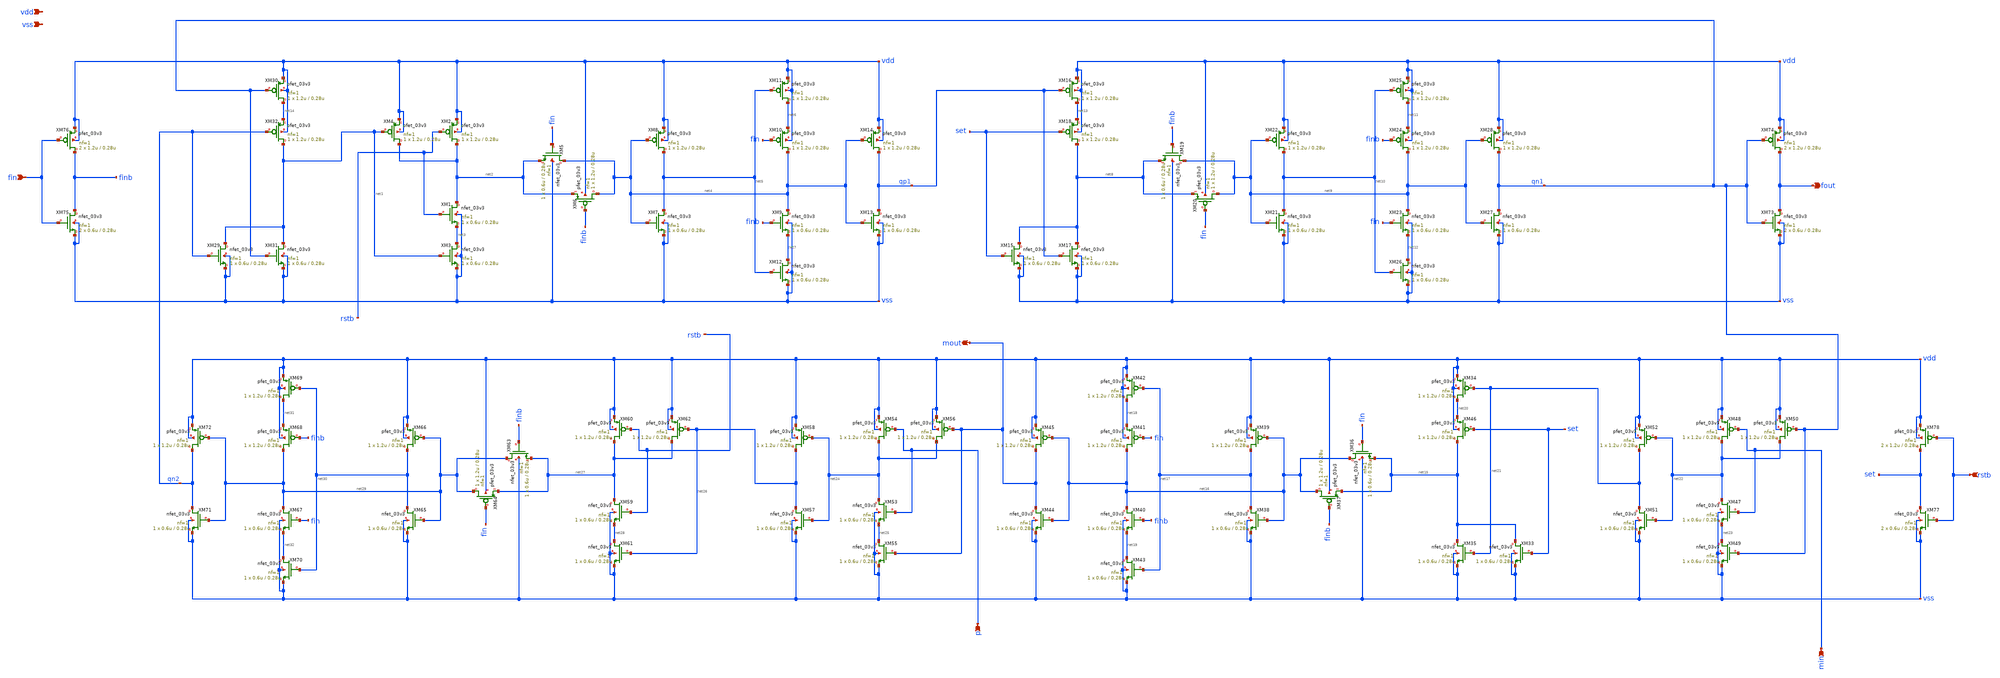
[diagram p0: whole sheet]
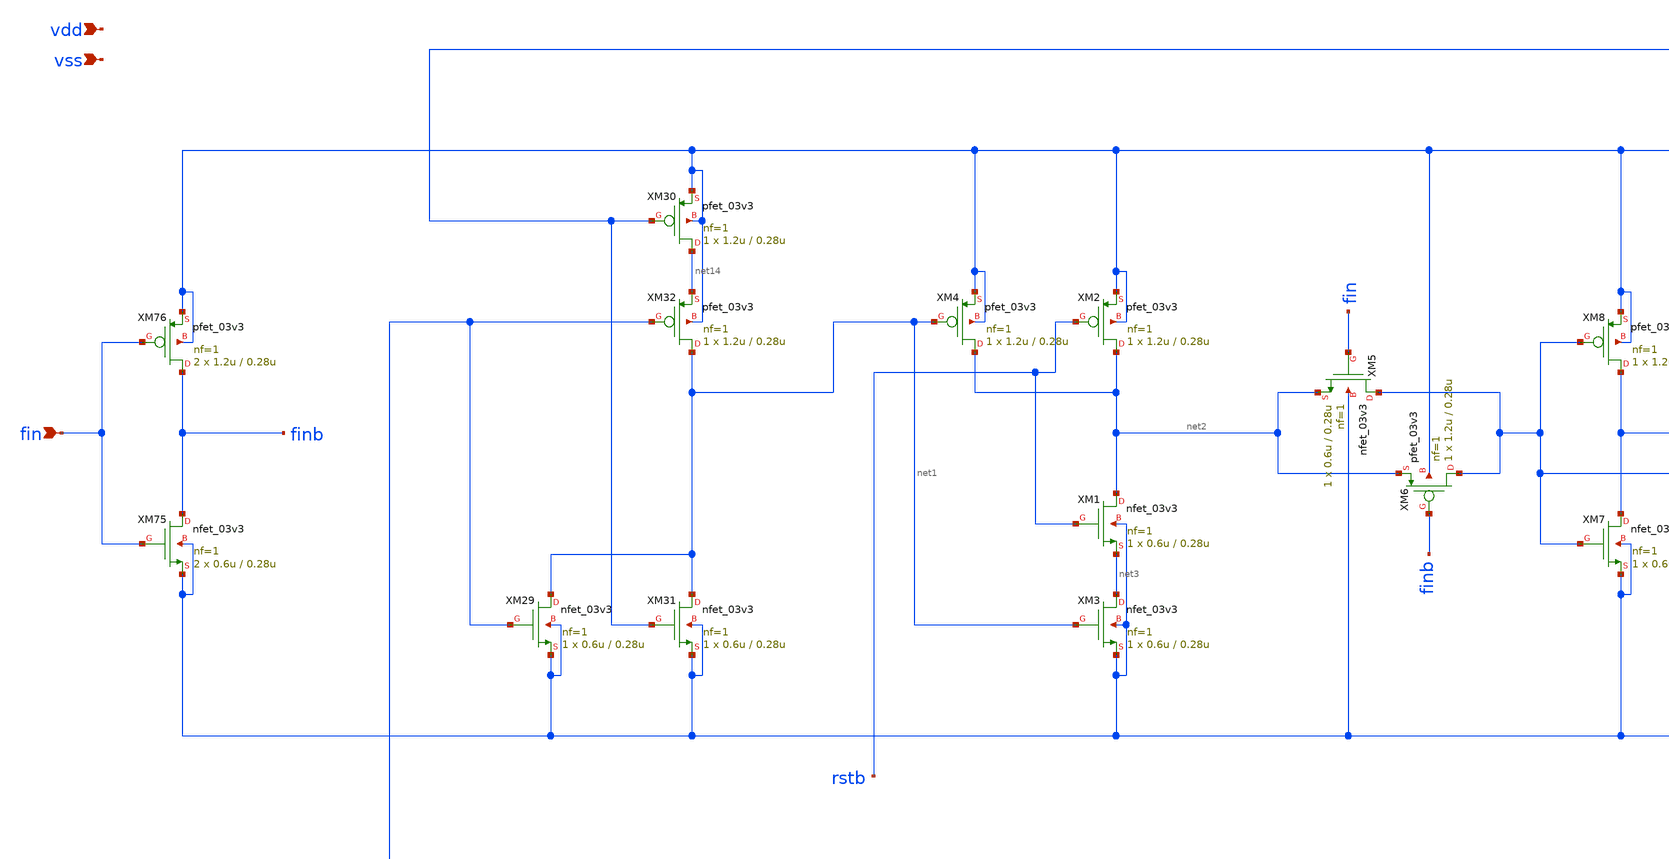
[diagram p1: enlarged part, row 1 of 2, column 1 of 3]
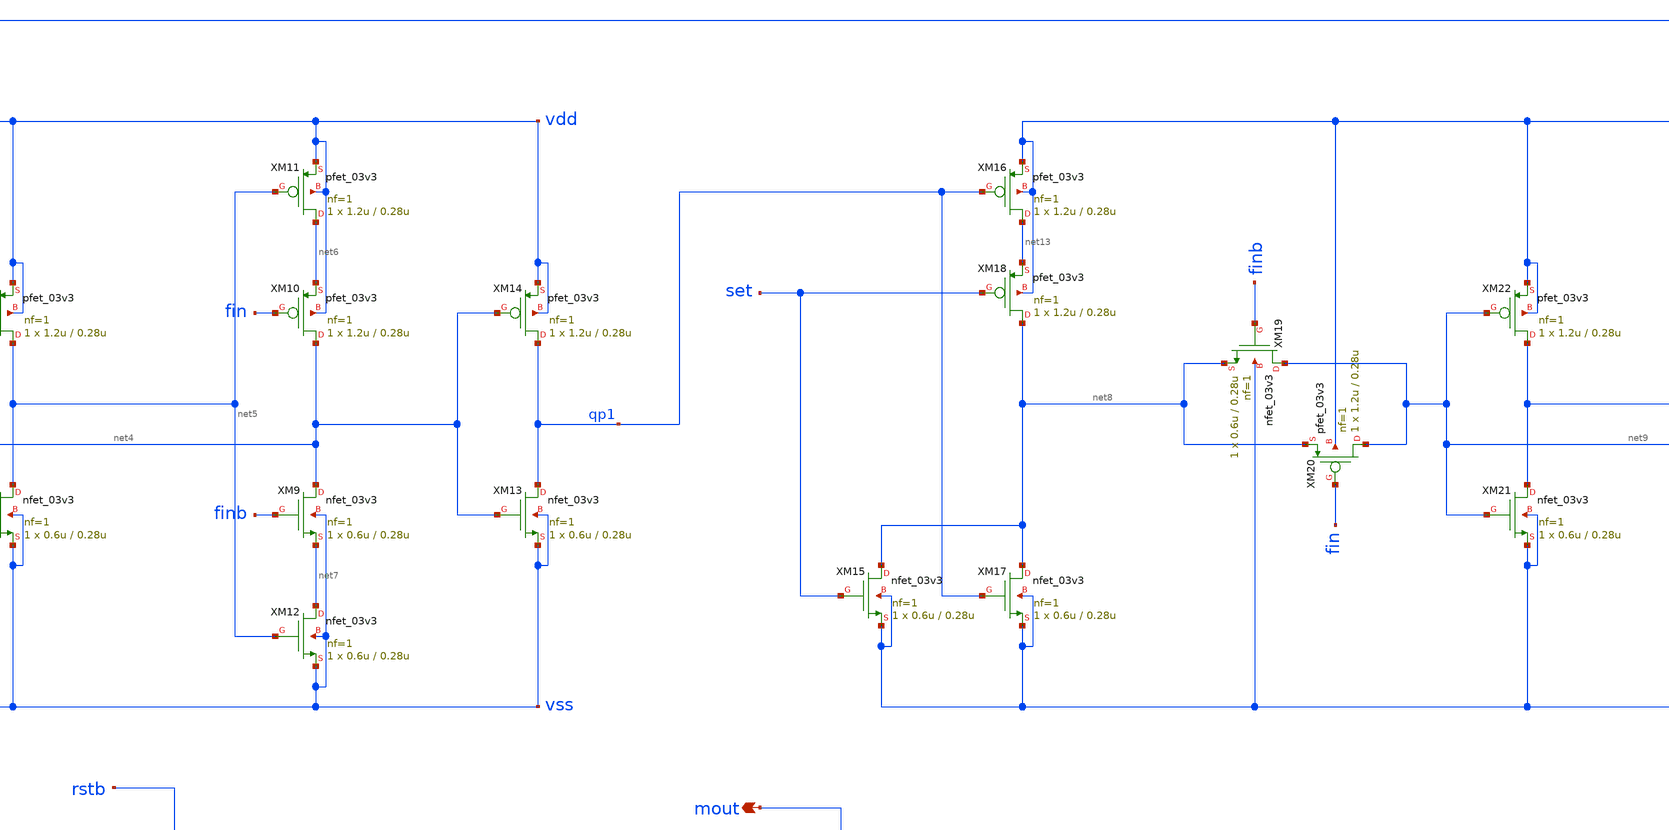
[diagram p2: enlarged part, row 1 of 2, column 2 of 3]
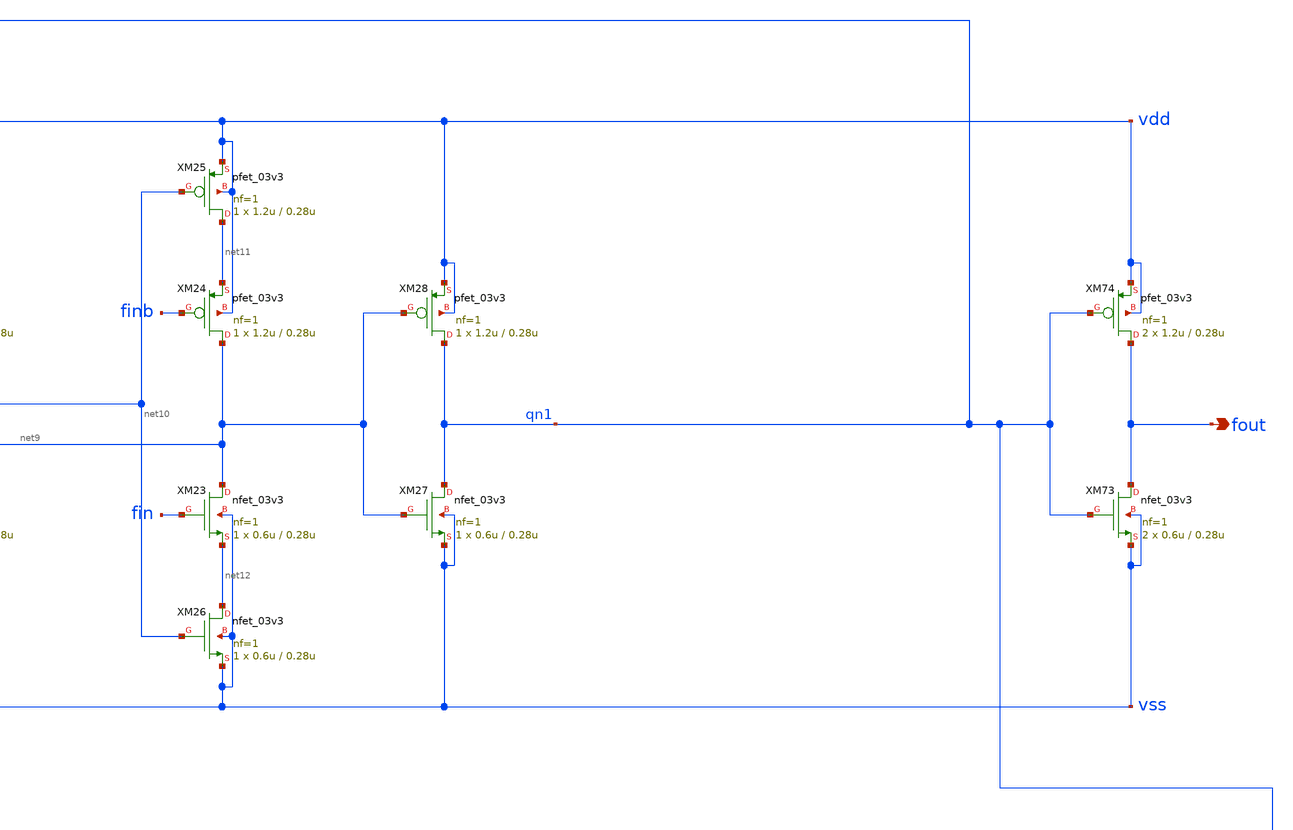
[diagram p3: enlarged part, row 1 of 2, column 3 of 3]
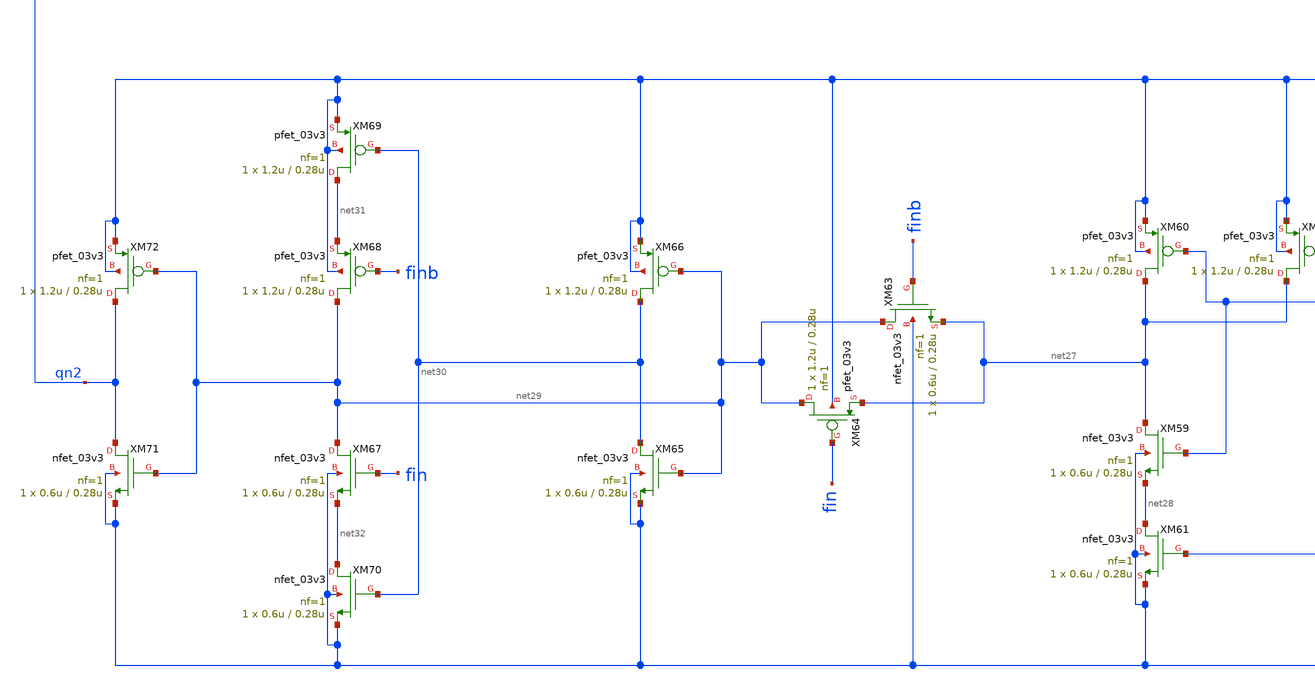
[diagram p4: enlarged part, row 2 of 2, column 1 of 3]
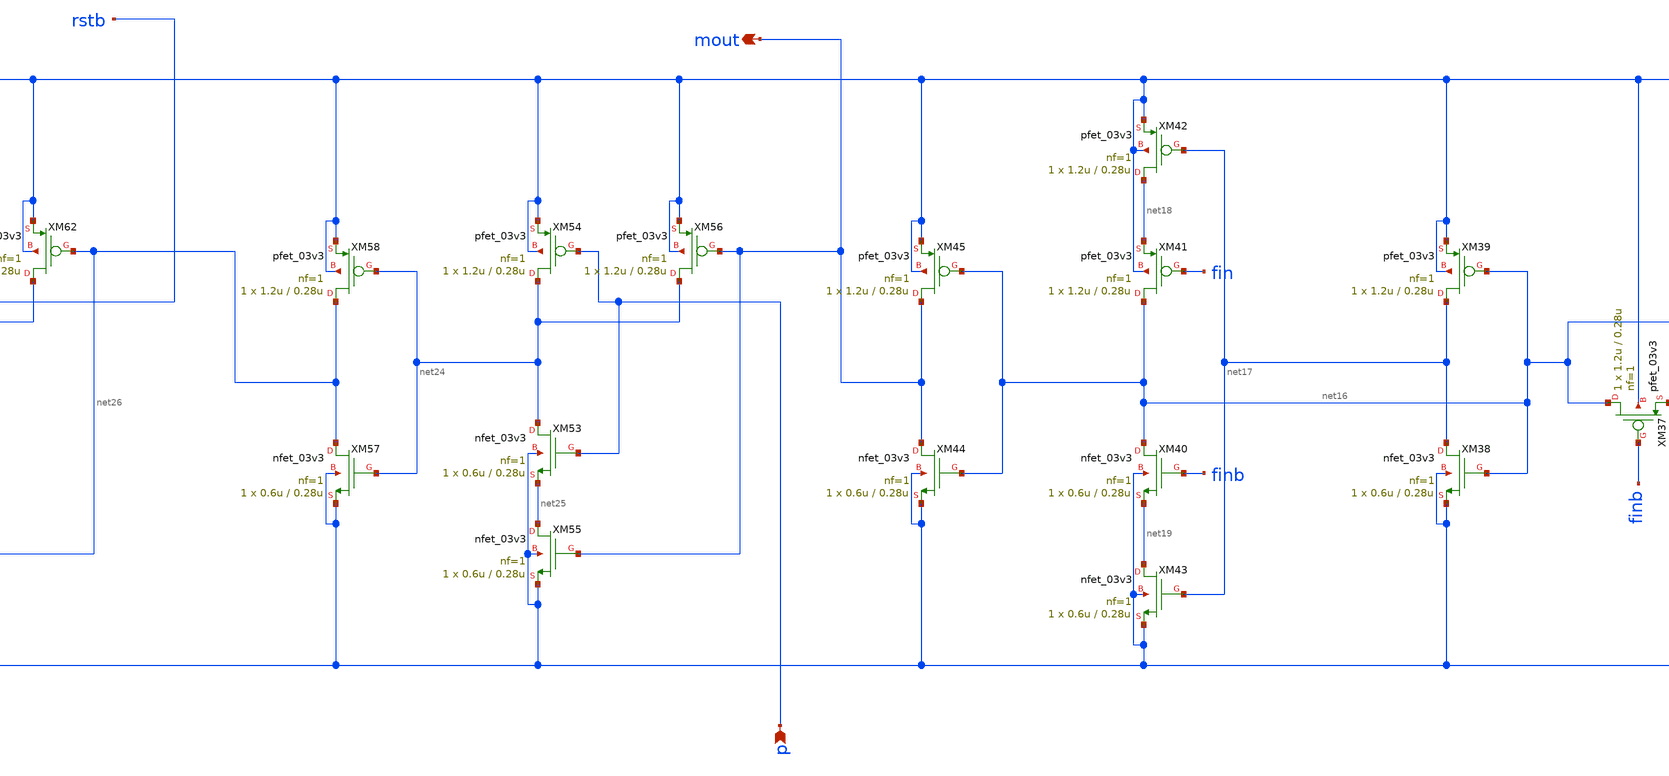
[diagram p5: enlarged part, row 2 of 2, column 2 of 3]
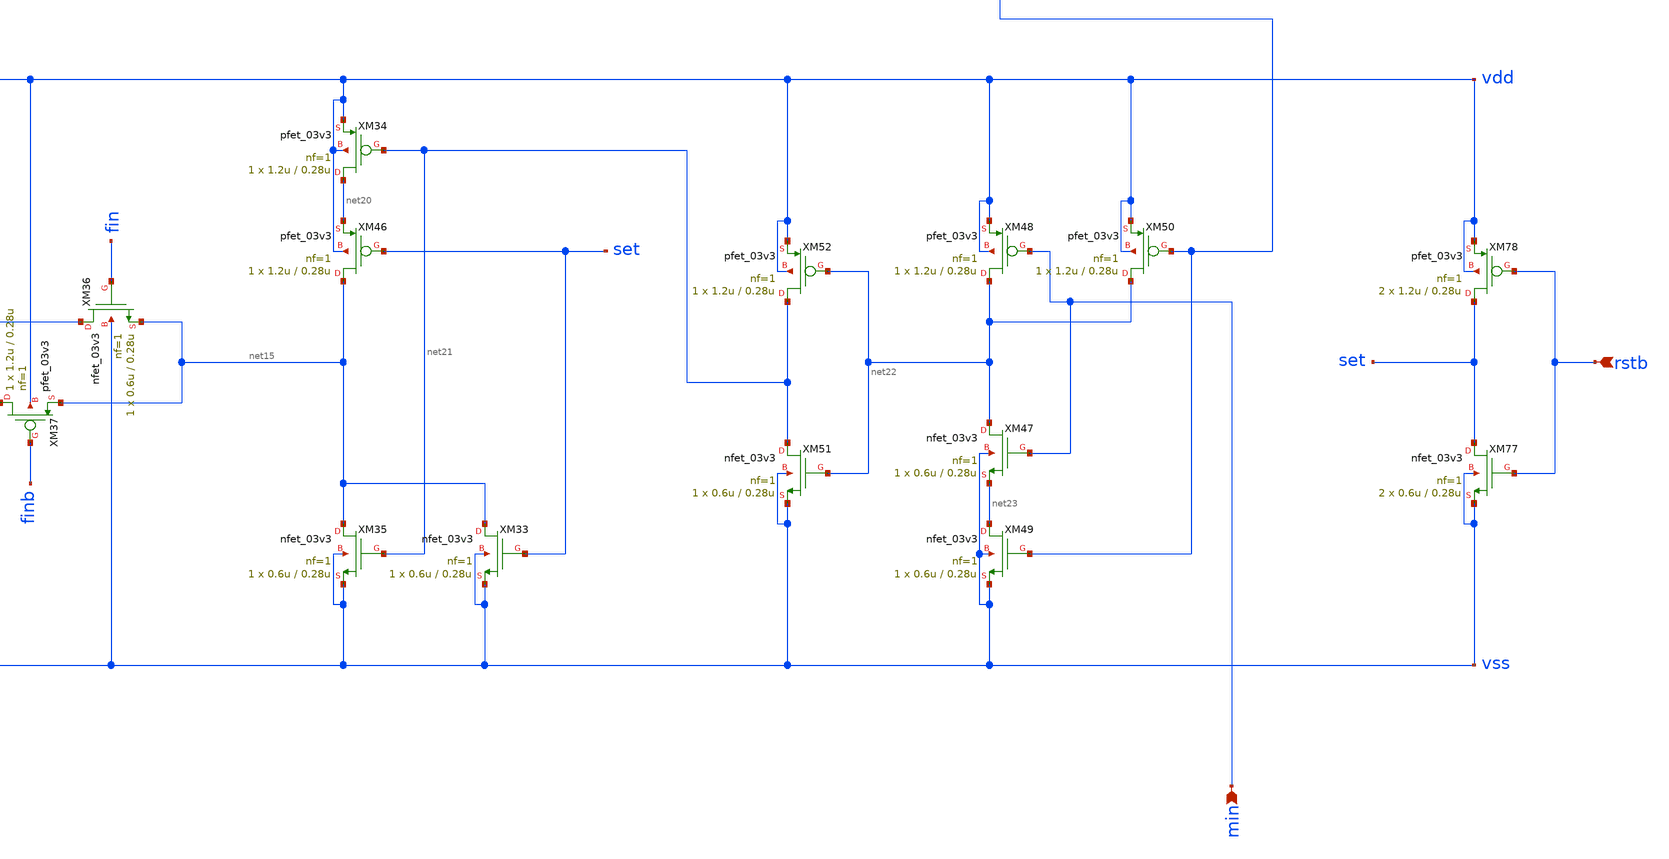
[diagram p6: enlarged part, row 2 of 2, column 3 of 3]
** sch_path: xschem/div23.sch
**.subckt div23 rstb fin p min fout mout vdd vss
*.ipin rstb
*.ipin fin
*.ipin p
*.ipin min
*.opin fout
*.opin mout
*.ipin vdd
*.ipin vss
XM1 net2 rstb net3 vss nfet_03v3 L=0.28u W=0.6u nf=1 ad='int((nf+1)/2) * W/nf * 0.18u' as='int((nf+2)/2) * W/nf * 0.18u'
+ pd='2*int((nf+1)/2) * (W/nf + 0.18u)' ps='2*int((nf+2)/2) * (W/nf + 0.18u)' nrd='0.18u / W' nrs='0.18u / W'
+ sa=0 sb=0 sd=0 m=1
XM2 net2 rstb vdd vdd pfet_03v3 L=0.28u W=1.2u nf=1 ad='int((nf+1)/2) * W/nf * 0.18u' as='int((nf+2)/2) * W/nf * 0.18u'
+ pd='2*int((nf+1)/2) * (W/nf + 0.18u)' ps='2*int((nf+2)/2) * (W/nf + 0.18u)' nrd='0.18u / W' nrs='0.18u / W'
+ sa=0 sb=0 sd=0 m=1
XM3 net3 net1 vss vss nfet_03v3 L=0.28u W=0.6u nf=1 ad='int((nf+1)/2) * W/nf * 0.18u' as='int((nf+2)/2) * W/nf * 0.18u'
+ pd='2*int((nf+1)/2) * (W/nf + 0.18u)' ps='2*int((nf+2)/2) * (W/nf + 0.18u)' nrd='0.18u / W' nrs='0.18u / W'
+ sa=0 sb=0 sd=0 m=1
XM4 net2 net1 vdd vdd pfet_03v3 L=0.28u W=1.2u nf=1 ad='int((nf+1)/2) * W/nf * 0.18u' as='int((nf+2)/2) * W/nf * 0.18u'
+ pd='2*int((nf+1)/2) * (W/nf + 0.18u)' ps='2*int((nf+2)/2) * (W/nf + 0.18u)' nrd='0.18u / W' nrs='0.18u / W'
+ sa=0 sb=0 sd=0 m=1
XM5 net4 fin net2 vss nfet_03v3 L=0.28u W=0.6u nf=1 ad='int((nf+1)/2) * W/nf * 0.18u' as='int((nf+2)/2) * W/nf * 0.18u'
+ pd='2*int((nf+1)/2) * (W/nf + 0.18u)' ps='2*int((nf+2)/2) * (W/nf + 0.18u)' nrd='0.18u / W' nrs='0.18u / W'
+ sa=0 sb=0 sd=0 m=1
XM6 net4 finb net2 vdd pfet_03v3 L=0.28u W=1.2u nf=1 ad='int((nf+1)/2) * W/nf * 0.18u' as='int((nf+2)/2) * W/nf * 0.18u'
+ pd='2*int((nf+1)/2) * (W/nf + 0.18u)' ps='2*int((nf+2)/2) * (W/nf + 0.18u)' nrd='0.18u / W' nrs='0.18u / W'
+ sa=0 sb=0 sd=0 m=1
XM7 net5 net4 vss vss nfet_03v3 L=0.28u W=0.6u nf=1 ad='int((nf+1)/2) * W/nf * 0.18u' as='int((nf+2)/2) * W/nf * 0.18u'
+ pd='2*int((nf+1)/2) * (W/nf + 0.18u)' ps='2*int((nf+2)/2) * (W/nf + 0.18u)' nrd='0.18u / W' nrs='0.18u / W'
+ sa=0 sb=0 sd=0 m=1
XM8 net5 net4 vdd vdd pfet_03v3 L=0.28u W=1.2u nf=1 ad='int((nf+1)/2) * W/nf * 0.18u' as='int((nf+2)/2) * W/nf * 0.18u'
+ pd='2*int((nf+1)/2) * (W/nf + 0.18u)' ps='2*int((nf+2)/2) * (W/nf + 0.18u)' nrd='0.18u / W' nrs='0.18u / W'
+ sa=0 sb=0 sd=0 m=1
XM9 net4 finb net7 vss nfet_03v3 L=0.28u W=0.6u nf=1 ad='int((nf+1)/2) * W/nf * 0.18u' as='int((nf+2)/2) * W/nf * 0.18u'
+ pd='2*int((nf+1)/2) * (W/nf + 0.18u)' ps='2*int((nf+2)/2) * (W/nf + 0.18u)' nrd='0.18u / W' nrs='0.18u / W'
+ sa=0 sb=0 sd=0 m=1
XM10 net4 fin net6 vdd pfet_03v3 L=0.28u W=1.2u nf=1 ad='int((nf+1)/2) * W/nf * 0.18u' as='int((nf+2)/2) * W/nf * 0.18u'
+ pd='2*int((nf+1)/2) * (W/nf + 0.18u)' ps='2*int((nf+2)/2) * (W/nf + 0.18u)' nrd='0.18u / W' nrs='0.18u / W'
+ sa=0 sb=0 sd=0 m=1
XM11 net6 net5 vdd vdd pfet_03v3 L=0.28u W=1.2u nf=1 ad='int((nf+1)/2) * W/nf * 0.18u' as='int((nf+2)/2) * W/nf * 0.18u'
+ pd='2*int((nf+1)/2) * (W/nf + 0.18u)' ps='2*int((nf+2)/2) * (W/nf + 0.18u)' nrd='0.18u / W' nrs='0.18u / W'
+ sa=0 sb=0 sd=0 m=1
XM12 net7 net5 vss vss nfet_03v3 L=0.28u W=0.6u nf=1 ad='int((nf+1)/2) * W/nf * 0.18u' as='int((nf+2)/2) * W/nf * 0.18u'
+ pd='2*int((nf+1)/2) * (W/nf + 0.18u)' ps='2*int((nf+2)/2) * (W/nf + 0.18u)' nrd='0.18u / W' nrs='0.18u / W'
+ sa=0 sb=0 sd=0 m=1
XM13 qp1 net4 vss vss nfet_03v3 L=0.28u W=0.6u nf=1 ad='int((nf+1)/2) * W/nf * 0.18u' as='int((nf+2)/2) * W/nf * 0.18u'
+ pd='2*int((nf+1)/2) * (W/nf + 0.18u)' ps='2*int((nf+2)/2) * (W/nf + 0.18u)' nrd='0.18u / W' nrs='0.18u / W'
+ sa=0 sb=0 sd=0 m=1
XM14 qp1 net4 vdd vdd pfet_03v3 L=0.28u W=1.2u nf=1 ad='int((nf+1)/2) * W/nf * 0.18u' as='int((nf+2)/2) * W/nf * 0.18u'
+ pd='2*int((nf+1)/2) * (W/nf + 0.18u)' ps='2*int((nf+2)/2) * (W/nf + 0.18u)' nrd='0.18u / W' nrs='0.18u / W'
+ sa=0 sb=0 sd=0 m=1
XM15 net8 set vss vss nfet_03v3 L=0.28u W=0.6u nf=1 ad='int((nf+1)/2) * W/nf * 0.18u' as='int((nf+2)/2) * W/nf * 0.18u'
+ pd='2*int((nf+1)/2) * (W/nf + 0.18u)' ps='2*int((nf+2)/2) * (W/nf + 0.18u)' nrd='0.18u / W' nrs='0.18u / W'
+ sa=0 sb=0 sd=0 m=1
XM16 net13 qp1 vdd vdd pfet_03v3 L=0.28u W=1.2u nf=1 ad='int((nf+1)/2) * W/nf * 0.18u' as='int((nf+2)/2) * W/nf * 0.18u'
+ pd='2*int((nf+1)/2) * (W/nf + 0.18u)' ps='2*int((nf+2)/2) * (W/nf + 0.18u)' nrd='0.18u / W' nrs='0.18u / W'
+ sa=0 sb=0 sd=0 m=1
XM17 net8 qp1 vss vss nfet_03v3 L=0.28u W=0.6u nf=1 ad='int((nf+1)/2) * W/nf * 0.18u' as='int((nf+2)/2) * W/nf * 0.18u'
+ pd='2*int((nf+1)/2) * (W/nf + 0.18u)' ps='2*int((nf+2)/2) * (W/nf + 0.18u)' nrd='0.18u / W' nrs='0.18u / W'
+ sa=0 sb=0 sd=0 m=1
XM19 net9 finb net8 vss nfet_03v3 L=0.28u W=0.6u nf=1 ad='int((nf+1)/2) * W/nf * 0.18u' as='int((nf+2)/2) * W/nf * 0.18u'
+ pd='2*int((nf+1)/2) * (W/nf + 0.18u)' ps='2*int((nf+2)/2) * (W/nf + 0.18u)' nrd='0.18u / W' nrs='0.18u / W'
+ sa=0 sb=0 sd=0 m=1
XM20 net9 fin net8 vdd pfet_03v3 L=0.28u W=1.2u nf=1 ad='int((nf+1)/2) * W/nf * 0.18u' as='int((nf+2)/2) * W/nf * 0.18u'
+ pd='2*int((nf+1)/2) * (W/nf + 0.18u)' ps='2*int((nf+2)/2) * (W/nf + 0.18u)' nrd='0.18u / W' nrs='0.18u / W'
+ sa=0 sb=0 sd=0 m=1
XM21 net10 net9 vss vss nfet_03v3 L=0.28u W=0.6u nf=1 ad='int((nf+1)/2) * W/nf * 0.18u' as='int((nf+2)/2) * W/nf * 0.18u'
+ pd='2*int((nf+1)/2) * (W/nf + 0.18u)' ps='2*int((nf+2)/2) * (W/nf + 0.18u)' nrd='0.18u / W' nrs='0.18u / W'
+ sa=0 sb=0 sd=0 m=1
XM22 net10 net9 vdd vdd pfet_03v3 L=0.28u W=1.2u nf=1 ad='int((nf+1)/2) * W/nf * 0.18u' as='int((nf+2)/2) * W/nf * 0.18u'
+ pd='2*int((nf+1)/2) * (W/nf + 0.18u)' ps='2*int((nf+2)/2) * (W/nf + 0.18u)' nrd='0.18u / W' nrs='0.18u / W'
+ sa=0 sb=0 sd=0 m=1
XM23 net9 fin net12 vss nfet_03v3 L=0.28u W=0.6u nf=1 ad='int((nf+1)/2) * W/nf * 0.18u' as='int((nf+2)/2) * W/nf * 0.18u'
+ pd='2*int((nf+1)/2) * (W/nf + 0.18u)' ps='2*int((nf+2)/2) * (W/nf + 0.18u)' nrd='0.18u / W' nrs='0.18u / W'
+ sa=0 sb=0 sd=0 m=1
XM24 net9 finb net11 vdd pfet_03v3 L=0.28u W=1.2u nf=1 ad='int((nf+1)/2) * W/nf * 0.18u' as='int((nf+2)/2) * W/nf * 0.18u'
+ pd='2*int((nf+1)/2) * (W/nf + 0.18u)' ps='2*int((nf+2)/2) * (W/nf + 0.18u)' nrd='0.18u / W' nrs='0.18u / W'
+ sa=0 sb=0 sd=0 m=1
XM25 net11 net10 vdd vdd pfet_03v3 L=0.28u W=1.2u nf=1 ad='int((nf+1)/2) * W/nf * 0.18u' as='int((nf+2)/2) * W/nf * 0.18u'
+ pd='2*int((nf+1)/2) * (W/nf + 0.18u)' ps='2*int((nf+2)/2) * (W/nf + 0.18u)' nrd='0.18u / W' nrs='0.18u / W'
+ sa=0 sb=0 sd=0 m=1
XM26 net12 net10 vss vss nfet_03v3 L=0.28u W=0.6u nf=1 ad='int((nf+1)/2) * W/nf * 0.18u' as='int((nf+2)/2) * W/nf * 0.18u'
+ pd='2*int((nf+1)/2) * (W/nf + 0.18u)' ps='2*int((nf+2)/2) * (W/nf + 0.18u)' nrd='0.18u / W' nrs='0.18u / W'
+ sa=0 sb=0 sd=0 m=1
XM27 qn1 net9 vss vss nfet_03v3 L=0.28u W=0.6u nf=1 ad='int((nf+1)/2) * W/nf * 0.18u' as='int((nf+2)/2) * W/nf * 0.18u'
+ pd='2*int((nf+1)/2) * (W/nf + 0.18u)' ps='2*int((nf+2)/2) * (W/nf + 0.18u)' nrd='0.18u / W' nrs='0.18u / W'
+ sa=0 sb=0 sd=0 m=1
XM28 qn1 net9 vdd vdd pfet_03v3 L=0.28u W=1.2u nf=1 ad='int((nf+1)/2) * W/nf * 0.18u' as='int((nf+2)/2) * W/nf * 0.18u'
+ pd='2*int((nf+1)/2) * (W/nf + 0.18u)' ps='2*int((nf+2)/2) * (W/nf + 0.18u)' nrd='0.18u / W' nrs='0.18u / W'
+ sa=0 sb=0 sd=0 m=1
XM18 net8 set net13 vdd pfet_03v3 L=0.28u W=1.2u nf=1 ad='int((nf+1)/2) * W/nf * 0.18u' as='int((nf+2)/2) * W/nf * 0.18u'
+ pd='2*int((nf+1)/2) * (W/nf + 0.18u)' ps='2*int((nf+2)/2) * (W/nf + 0.18u)' nrd='0.18u / W' nrs='0.18u / W'
+ sa=0 sb=0 sd=0 m=1
XM29 net1 qn2 vss vss nfet_03v3 L=0.28u W=0.6u nf=1 ad='int((nf+1)/2) * W/nf * 0.18u' as='int((nf+2)/2) * W/nf * 0.18u'
+ pd='2*int((nf+1)/2) * (W/nf + 0.18u)' ps='2*int((nf+2)/2) * (W/nf + 0.18u)' nrd='0.18u / W' nrs='0.18u / W'
+ sa=0 sb=0 sd=0 m=1
XM30 net14 qn1 vdd vdd pfet_03v3 L=0.28u W=1.2u nf=1 ad='int((nf+1)/2) * W/nf * 0.18u' as='int((nf+2)/2) * W/nf * 0.18u'
+ pd='2*int((nf+1)/2) * (W/nf + 0.18u)' ps='2*int((nf+2)/2) * (W/nf + 0.18u)' nrd='0.18u / W' nrs='0.18u / W'
+ sa=0 sb=0 sd=0 m=1
XM31 net1 qn1 vss vss nfet_03v3 L=0.28u W=0.6u nf=1 ad='int((nf+1)/2) * W/nf * 0.18u' as='int((nf+2)/2) * W/nf * 0.18u'
+ pd='2*int((nf+1)/2) * (W/nf + 0.18u)' ps='2*int((nf+2)/2) * (W/nf + 0.18u)' nrd='0.18u / W' nrs='0.18u / W'
+ sa=0 sb=0 sd=0 m=1
XM32 net1 qn2 net14 vdd pfet_03v3 L=0.28u W=1.2u nf=1 ad='int((nf+1)/2) * W/nf * 0.18u' as='int((nf+2)/2) * W/nf * 0.18u'
+ pd='2*int((nf+1)/2) * (W/nf + 0.18u)' ps='2*int((nf+2)/2) * (W/nf + 0.18u)' nrd='0.18u / W' nrs='0.18u / W'
+ sa=0 sb=0 sd=0 m=1
XM33 net15 set vss vss nfet_03v3 L=0.28u W=0.6u nf=1 ad='int((nf+1)/2) * W/nf * 0.18u' as='int((nf+2)/2) * W/nf * 0.18u'
+ pd='2*int((nf+1)/2) * (W/nf + 0.18u)' ps='2*int((nf+2)/2) * (W/nf + 0.18u)' nrd='0.18u / W' nrs='0.18u / W'
+ sa=0 sb=0 sd=0 m=1
XM34 net20 net21 vdd vdd pfet_03v3 L=0.28u W=1.2u nf=1 ad='int((nf+1)/2) * W/nf * 0.18u' as='int((nf+2)/2) * W/nf * 0.18u'
+ pd='2*int((nf+1)/2) * (W/nf + 0.18u)' ps='2*int((nf+2)/2) * (W/nf + 0.18u)' nrd='0.18u / W' nrs='0.18u / W'
+ sa=0 sb=0 sd=0 m=1
XM35 net15 net21 vss vss nfet_03v3 L=0.28u W=0.6u nf=1 ad='int((nf+1)/2) * W/nf * 0.18u' as='int((nf+2)/2) * W/nf * 0.18u'
+ pd='2*int((nf+1)/2) * (W/nf + 0.18u)' ps='2*int((nf+2)/2) * (W/nf + 0.18u)' nrd='0.18u / W' nrs='0.18u / W'
+ sa=0 sb=0 sd=0 m=1
XM36 net16 fin net15 vss nfet_03v3 L=0.28u W=0.6u nf=1 ad='int((nf+1)/2) * W/nf * 0.18u' as='int((nf+2)/2) * W/nf * 0.18u'
+ pd='2*int((nf+1)/2) * (W/nf + 0.18u)' ps='2*int((nf+2)/2) * (W/nf + 0.18u)' nrd='0.18u / W' nrs='0.18u / W'
+ sa=0 sb=0 sd=0 m=1
XM37 net16 finb net15 vdd pfet_03v3 L=0.28u W=1.2u nf=1 ad='int((nf+1)/2) * W/nf * 0.18u' as='int((nf+2)/2) * W/nf * 0.18u'
+ pd='2*int((nf+1)/2) * (W/nf + 0.18u)' ps='2*int((nf+2)/2) * (W/nf + 0.18u)' nrd='0.18u / W' nrs='0.18u / W'
+ sa=0 sb=0 sd=0 m=1
XM38 net17 net16 vss vss nfet_03v3 L=0.28u W=0.6u nf=1 ad='int((nf+1)/2) * W/nf * 0.18u' as='int((nf+2)/2) * W/nf * 0.18u'
+ pd='2*int((nf+1)/2) * (W/nf + 0.18u)' ps='2*int((nf+2)/2) * (W/nf + 0.18u)' nrd='0.18u / W' nrs='0.18u / W'
+ sa=0 sb=0 sd=0 m=1
XM39 net17 net16 vdd vdd pfet_03v3 L=0.28u W=1.2u nf=1 ad='int((nf+1)/2) * W/nf * 0.18u' as='int((nf+2)/2) * W/nf * 0.18u'
+ pd='2*int((nf+1)/2) * (W/nf + 0.18u)' ps='2*int((nf+2)/2) * (W/nf + 0.18u)' nrd='0.18u / W' nrs='0.18u / W'
+ sa=0 sb=0 sd=0 m=1
XM40 net16 finb net19 vss nfet_03v3 L=0.28u W=0.6u nf=1 ad='int((nf+1)/2) * W/nf * 0.18u' as='int((nf+2)/2) * W/nf * 0.18u'
+ pd='2*int((nf+1)/2) * (W/nf + 0.18u)' ps='2*int((nf+2)/2) * (W/nf + 0.18u)' nrd='0.18u / W' nrs='0.18u / W'
+ sa=0 sb=0 sd=0 m=1
XM41 net16 fin net18 vdd pfet_03v3 L=0.28u W=1.2u nf=1 ad='int((nf+1)/2) * W/nf * 0.18u' as='int((nf+2)/2) * W/nf * 0.18u'
+ pd='2*int((nf+1)/2) * (W/nf + 0.18u)' ps='2*int((nf+2)/2) * (W/nf + 0.18u)' nrd='0.18u / W' nrs='0.18u / W'
+ sa=0 sb=0 sd=0 m=1
XM42 net18 net17 vdd vdd pfet_03v3 L=0.28u W=1.2u nf=1 ad='int((nf+1)/2) * W/nf * 0.18u' as='int((nf+2)/2) * W/nf * 0.18u'
+ pd='2*int((nf+1)/2) * (W/nf + 0.18u)' ps='2*int((nf+2)/2) * (W/nf + 0.18u)' nrd='0.18u / W' nrs='0.18u / W'
+ sa=0 sb=0 sd=0 m=1
XM43 net19 net17 vss vss nfet_03v3 L=0.28u W=0.6u nf=1 ad='int((nf+1)/2) * W/nf * 0.18u' as='int((nf+2)/2) * W/nf * 0.18u'
+ pd='2*int((nf+1)/2) * (W/nf + 0.18u)' ps='2*int((nf+2)/2) * (W/nf + 0.18u)' nrd='0.18u / W' nrs='0.18u / W'
+ sa=0 sb=0 sd=0 m=1
XM44 mout net16 vss vss nfet_03v3 L=0.28u W=0.6u nf=1 ad='int((nf+1)/2) * W/nf * 0.18u' as='int((nf+2)/2) * W/nf * 0.18u'
+ pd='2*int((nf+1)/2) * (W/nf + 0.18u)' ps='2*int((nf+2)/2) * (W/nf + 0.18u)' nrd='0.18u / W' nrs='0.18u / W'
+ sa=0 sb=0 sd=0 m=1
XM45 mout net16 vdd vdd pfet_03v3 L=0.28u W=1.2u nf=1 ad='int((nf+1)/2) * W/nf * 0.18u' as='int((nf+2)/2) * W/nf * 0.18u'
+ pd='2*int((nf+1)/2) * (W/nf + 0.18u)' ps='2*int((nf+2)/2) * (W/nf + 0.18u)' nrd='0.18u / W' nrs='0.18u / W'
+ sa=0 sb=0 sd=0 m=1
XM46 net15 set net20 vdd pfet_03v3 L=0.28u W=1.2u nf=1 ad='int((nf+1)/2) * W/nf * 0.18u' as='int((nf+2)/2) * W/nf * 0.18u'
+ pd='2*int((nf+1)/2) * (W/nf + 0.18u)' ps='2*int((nf+2)/2) * (W/nf + 0.18u)' nrd='0.18u / W' nrs='0.18u / W'
+ sa=0 sb=0 sd=0 m=1
XM47 net22 min net23 vss nfet_03v3 L=0.28u W=0.6u nf=1 ad='int((nf+1)/2) * W/nf * 0.18u' as='int((nf+2)/2) * W/nf * 0.18u'
+ pd='2*int((nf+1)/2) * (W/nf + 0.18u)' ps='2*int((nf+2)/2) * (W/nf + 0.18u)' nrd='0.18u / W' nrs='0.18u / W'
+ sa=0 sb=0 sd=0 m=1
XM48 net22 min vdd vdd pfet_03v3 L=0.28u W=1.2u nf=1 ad='int((nf+1)/2) * W/nf * 0.18u' as='int((nf+2)/2) * W/nf * 0.18u'
+ pd='2*int((nf+1)/2) * (W/nf + 0.18u)' ps='2*int((nf+2)/2) * (W/nf + 0.18u)' nrd='0.18u / W' nrs='0.18u / W'
+ sa=0 sb=0 sd=0 m=1
XM49 net23 qn1 vss vss nfet_03v3 L=0.28u W=0.6u nf=1 ad='int((nf+1)/2) * W/nf * 0.18u' as='int((nf+2)/2) * W/nf * 0.18u'
+ pd='2*int((nf+1)/2) * (W/nf + 0.18u)' ps='2*int((nf+2)/2) * (W/nf + 0.18u)' nrd='0.18u / W' nrs='0.18u / W'
+ sa=0 sb=0 sd=0 m=1
XM50 net22 qn1 vdd vdd pfet_03v3 L=0.28u W=1.2u nf=1 ad='int((nf+1)/2) * W/nf * 0.18u' as='int((nf+2)/2) * W/nf * 0.18u'
+ pd='2*int((nf+1)/2) * (W/nf + 0.18u)' ps='2*int((nf+2)/2) * (W/nf + 0.18u)' nrd='0.18u / W' nrs='0.18u / W'
+ sa=0 sb=0 sd=0 m=1
XM51 net21 net22 vss vss nfet_03v3 L=0.28u W=0.6u nf=1 ad='int((nf+1)/2) * W/nf * 0.18u' as='int((nf+2)/2) * W/nf * 0.18u'
+ pd='2*int((nf+1)/2) * (W/nf + 0.18u)' ps='2*int((nf+2)/2) * (W/nf + 0.18u)' nrd='0.18u / W' nrs='0.18u / W'
+ sa=0 sb=0 sd=0 m=1
XM52 net21 net22 vdd vdd pfet_03v3 L=0.28u W=1.2u nf=1 ad='int((nf+1)/2) * W/nf * 0.18u' as='int((nf+2)/2) * W/nf * 0.18u'
+ pd='2*int((nf+1)/2) * (W/nf + 0.18u)' ps='2*int((nf+2)/2) * (W/nf + 0.18u)' nrd='0.18u / W' nrs='0.18u / W'
+ sa=0 sb=0 sd=0 m=1
XM53 net24 p net25 vss nfet_03v3 L=0.28u W=0.6u nf=1 ad='int((nf+1)/2) * W/nf * 0.18u' as='int((nf+2)/2) * W/nf * 0.18u'
+ pd='2*int((nf+1)/2) * (W/nf + 0.18u)' ps='2*int((nf+2)/2) * (W/nf + 0.18u)' nrd='0.18u / W' nrs='0.18u / W'
+ sa=0 sb=0 sd=0 m=1
XM54 net24 p vdd vdd pfet_03v3 L=0.28u W=1.2u nf=1 ad='int((nf+1)/2) * W/nf * 0.18u' as='int((nf+2)/2) * W/nf * 0.18u'
+ pd='2*int((nf+1)/2) * (W/nf + 0.18u)' ps='2*int((nf+2)/2) * (W/nf + 0.18u)' nrd='0.18u / W' nrs='0.18u / W'
+ sa=0 sb=0 sd=0 m=1
XM55 net25 mout vss vss nfet_03v3 L=0.28u W=0.6u nf=1 ad='int((nf+1)/2) * W/nf * 0.18u' as='int((nf+2)/2) * W/nf * 0.18u'
+ pd='2*int((nf+1)/2) * (W/nf + 0.18u)' ps='2*int((nf+2)/2) * (W/nf + 0.18u)' nrd='0.18u / W' nrs='0.18u / W'
+ sa=0 sb=0 sd=0 m=1
XM56 net24 mout vdd vdd pfet_03v3 L=0.28u W=1.2u nf=1 ad='int((nf+1)/2) * W/nf * 0.18u' as='int((nf+2)/2) * W/nf * 0.18u'
+ pd='2*int((nf+1)/2) * (W/nf + 0.18u)' ps='2*int((nf+2)/2) * (W/nf + 0.18u)' nrd='0.18u / W' nrs='0.18u / W'
+ sa=0 sb=0 sd=0 m=1
XM57 net26 net24 vss vss nfet_03v3 L=0.28u W=0.6u nf=1 ad='int((nf+1)/2) * W/nf * 0.18u' as='int((nf+2)/2) * W/nf * 0.18u'
+ pd='2*int((nf+1)/2) * (W/nf + 0.18u)' ps='2*int((nf+2)/2) * (W/nf + 0.18u)' nrd='0.18u / W' nrs='0.18u / W'
+ sa=0 sb=0 sd=0 m=1
XM58 net26 net24 vdd vdd pfet_03v3 L=0.28u W=1.2u nf=1 ad='int((nf+1)/2) * W/nf * 0.18u' as='int((nf+2)/2) * W/nf * 0.18u'
+ pd='2*int((nf+1)/2) * (W/nf + 0.18u)' ps='2*int((nf+2)/2) * (W/nf + 0.18u)' nrd='0.18u / W' nrs='0.18u / W'
+ sa=0 sb=0 sd=0 m=1
XM59 net27 rstb net28 vss nfet_03v3 L=0.28u W=0.6u nf=1 ad='int((nf+1)/2) * W/nf * 0.18u' as='int((nf+2)/2) * W/nf * 0.18u'
+ pd='2*int((nf+1)/2) * (W/nf + 0.18u)' ps='2*int((nf+2)/2) * (W/nf + 0.18u)' nrd='0.18u / W' nrs='0.18u / W'
+ sa=0 sb=0 sd=0 m=1
XM60 net27 rstb vdd vdd pfet_03v3 L=0.28u W=1.2u nf=1 ad='int((nf+1)/2) * W/nf * 0.18u' as='int((nf+2)/2) * W/nf * 0.18u'
+ pd='2*int((nf+1)/2) * (W/nf + 0.18u)' ps='2*int((nf+2)/2) * (W/nf + 0.18u)' nrd='0.18u / W' nrs='0.18u / W'
+ sa=0 sb=0 sd=0 m=1
XM61 net28 net26 vss vss nfet_03v3 L=0.28u W=0.6u nf=1 ad='int((nf+1)/2) * W/nf * 0.18u' as='int((nf+2)/2) * W/nf * 0.18u'
+ pd='2*int((nf+1)/2) * (W/nf + 0.18u)' ps='2*int((nf+2)/2) * (W/nf + 0.18u)' nrd='0.18u / W' nrs='0.18u / W'
+ sa=0 sb=0 sd=0 m=1
XM62 net27 net26 vdd vdd pfet_03v3 L=0.28u W=1.2u nf=1 ad='int((nf+1)/2) * W/nf * 0.18u' as='int((nf+2)/2) * W/nf * 0.18u'
+ pd='2*int((nf+1)/2) * (W/nf + 0.18u)' ps='2*int((nf+2)/2) * (W/nf + 0.18u)' nrd='0.18u / W' nrs='0.18u / W'
+ sa=0 sb=0 sd=0 m=1
XM63 net29 finb net27 vss nfet_03v3 L=0.28u W=0.6u nf=1 ad='int((nf+1)/2) * W/nf * 0.18u' as='int((nf+2)/2) * W/nf * 0.18u'
+ pd='2*int((nf+1)/2) * (W/nf + 0.18u)' ps='2*int((nf+2)/2) * (W/nf + 0.18u)' nrd='0.18u / W' nrs='0.18u / W'
+ sa=0 sb=0 sd=0 m=1
XM64 net29 fin net27 vdd pfet_03v3 L=0.28u W=1.2u nf=1 ad='int((nf+1)/2) * W/nf * 0.18u' as='int((nf+2)/2) * W/nf * 0.18u'
+ pd='2*int((nf+1)/2) * (W/nf + 0.18u)' ps='2*int((nf+2)/2) * (W/nf + 0.18u)' nrd='0.18u / W' nrs='0.18u / W'
+ sa=0 sb=0 sd=0 m=1
XM65 net30 net29 vss vss nfet_03v3 L=0.28u W=0.6u nf=1 ad='int((nf+1)/2) * W/nf * 0.18u' as='int((nf+2)/2) * W/nf * 0.18u'
+ pd='2*int((nf+1)/2) * (W/nf + 0.18u)' ps='2*int((nf+2)/2) * (W/nf + 0.18u)' nrd='0.18u / W' nrs='0.18u / W'
+ sa=0 sb=0 sd=0 m=1
XM66 net30 net29 vdd vdd pfet_03v3 L=0.28u W=1.2u nf=1 ad='int((nf+1)/2) * W/nf * 0.18u' as='int((nf+2)/2) * W/nf * 0.18u'
+ pd='2*int((nf+1)/2) * (W/nf + 0.18u)' ps='2*int((nf+2)/2) * (W/nf + 0.18u)' nrd='0.18u / W' nrs='0.18u / W'
+ sa=0 sb=0 sd=0 m=1
XM67 net29 fin net32 vss nfet_03v3 L=0.28u W=0.6u nf=1 ad='int((nf+1)/2) * W/nf * 0.18u' as='int((nf+2)/2) * W/nf * 0.18u'
+ pd='2*int((nf+1)/2) * (W/nf + 0.18u)' ps='2*int((nf+2)/2) * (W/nf + 0.18u)' nrd='0.18u / W' nrs='0.18u / W'
+ sa=0 sb=0 sd=0 m=1
XM68 net29 finb net31 vdd pfet_03v3 L=0.28u W=1.2u nf=1 ad='int((nf+1)/2) * W/nf * 0.18u' as='int((nf+2)/2) * W/nf * 0.18u'
+ pd='2*int((nf+1)/2) * (W/nf + 0.18u)' ps='2*int((nf+2)/2) * (W/nf + 0.18u)' nrd='0.18u / W' nrs='0.18u / W'
+ sa=0 sb=0 sd=0 m=1
XM69 net31 net30 vdd vdd pfet_03v3 L=0.28u W=1.2u nf=1 ad='int((nf+1)/2) * W/nf * 0.18u' as='int((nf+2)/2) * W/nf * 0.18u'
+ pd='2*int((nf+1)/2) * (W/nf + 0.18u)' ps='2*int((nf+2)/2) * (W/nf + 0.18u)' nrd='0.18u / W' nrs='0.18u / W'
+ sa=0 sb=0 sd=0 m=1
XM70 net32 net30 vss vss nfet_03v3 L=0.28u W=0.6u nf=1 ad='int((nf+1)/2) * W/nf * 0.18u' as='int((nf+2)/2) * W/nf * 0.18u'
+ pd='2*int((nf+1)/2) * (W/nf + 0.18u)' ps='2*int((nf+2)/2) * (W/nf + 0.18u)' nrd='0.18u / W' nrs='0.18u / W'
+ sa=0 sb=0 sd=0 m=1
XM71 qn2 net29 vss vss nfet_03v3 L=0.28u W=0.6u nf=1 ad='int((nf+1)/2) * W/nf * 0.18u' as='int((nf+2)/2) * W/nf * 0.18u'
+ pd='2*int((nf+1)/2) * (W/nf + 0.18u)' ps='2*int((nf+2)/2) * (W/nf + 0.18u)' nrd='0.18u / W' nrs='0.18u / W'
+ sa=0 sb=0 sd=0 m=1
XM72 qn2 net29 vdd vdd pfet_03v3 L=0.28u W=1.2u nf=1 ad='int((nf+1)/2) * W/nf * 0.18u' as='int((nf+2)/2) * W/nf * 0.18u'
+ pd='2*int((nf+1)/2) * (W/nf + 0.18u)' ps='2*int((nf+2)/2) * (W/nf + 0.18u)' nrd='0.18u / W' nrs='0.18u / W'
+ sa=0 sb=0 sd=0 m=1
XM73 fout qn1 vss vss nfet_03v3 L=0.28u W=0.6u nf=1 ad='int((nf+1)/2) * W/nf * 0.18u' as='int((nf+2)/2) * W/nf * 0.18u'
+ pd='2*int((nf+1)/2) * (W/nf + 0.18u)' ps='2*int((nf+2)/2) * (W/nf + 0.18u)' nrd='0.18u / W' nrs='0.18u / W'
+ sa=0 sb=0 sd=0 m=2
XM74 fout qn1 vdd vdd pfet_03v3 L=0.28u W=1.2u nf=1 ad='int((nf+1)/2) * W/nf * 0.18u' as='int((nf+2)/2) * W/nf * 0.18u'
+ pd='2*int((nf+1)/2) * (W/nf + 0.18u)' ps='2*int((nf+2)/2) * (W/nf + 0.18u)' nrd='0.18u / W' nrs='0.18u / W'
+ sa=0 sb=0 sd=0 m=2
XM75 finb fin vss vss nfet_03v3 L=0.28u W=0.6u nf=1 ad='int((nf+1)/2) * W/nf * 0.18u' as='int((nf+2)/2) * W/nf * 0.18u'
+ pd='2*int((nf+1)/2) * (W/nf + 0.18u)' ps='2*int((nf+2)/2) * (W/nf + 0.18u)' nrd='0.18u / W' nrs='0.18u / W'
+ sa=0 sb=0 sd=0 m=2
XM76 finb fin vdd vdd pfet_03v3 L=0.28u W=1.2u nf=1 ad='int((nf+1)/2) * W/nf * 0.18u' as='int((nf+2)/2) * W/nf * 0.18u'
+ pd='2*int((nf+1)/2) * (W/nf + 0.18u)' ps='2*int((nf+2)/2) * (W/nf + 0.18u)' nrd='0.18u / W' nrs='0.18u / W'
+ sa=0 sb=0 sd=0 m=2
XM77 set rstb vss vss nfet_03v3 L=0.28u W=0.6u nf=1 ad='int((nf+1)/2) * W/nf * 0.18u' as='int((nf+2)/2) * W/nf * 0.18u'
+ pd='2*int((nf+1)/2) * (W/nf + 0.18u)' ps='2*int((nf+2)/2) * (W/nf + 0.18u)' nrd='0.18u / W' nrs='0.18u / W'
+ sa=0 sb=0 sd=0 m=2
XM78 set rstb vdd vdd pfet_03v3 L=0.28u W=1.2u nf=1 ad='int((nf+1)/2) * W/nf * 0.18u' as='int((nf+2)/2) * W/nf * 0.18u'
+ pd='2*int((nf+1)/2) * (W/nf + 0.18u)' ps='2*int((nf+2)/2) * (W/nf + 0.18u)' nrd='0.18u / W' nrs='0.18u / W'
+ sa=0 sb=0 sd=0 m=2
**.ends
.end
